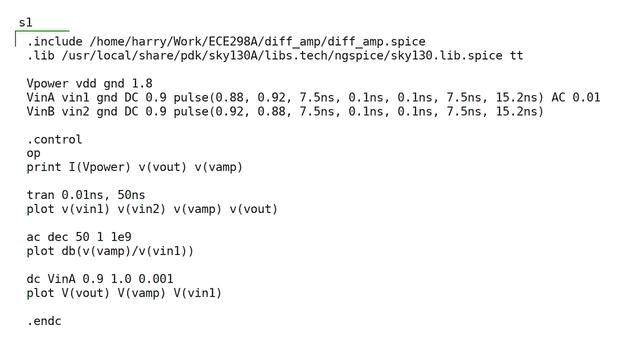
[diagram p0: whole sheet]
** sch_path: magic_xschem_ngspice/Magic_sim.sch
**.subckt Magic_sim
**** begin user architecture code

.include /home/harry/Work/ECE298A/diff_amp/diff_amp.spice
.lib /usr/local/share/pdk/sky130A/libs.tech/ngspice/sky130.lib.spice tt

Vpower vdd gnd 1.8
VinA vin1 gnd DC 0.9 pulse(0.88, 0.92, 7.5ns, 0.1ns, 0.1ns, 7.5ns, 15.2ns) AC 0.01
VinB vin2 gnd DC 0.9 pulse(0.92, 0.88, 7.5ns, 0.1ns, 0.1ns, 7.5ns, 15.2ns)

.control
op
print I(Vpower) v(vout) v(vamp)

tran 0.01ns, 50ns
plot v(vin1) v(vin2) v(vamp) v(vout)

ac dec 50 1 1e9
plot db(v(vamp)/v(vin1))

dc VinA 0.9 1.0 0.001
plot V(vout) V(vamp) V(vin1)

.endc

**** end user architecture code
**.ends
.end
